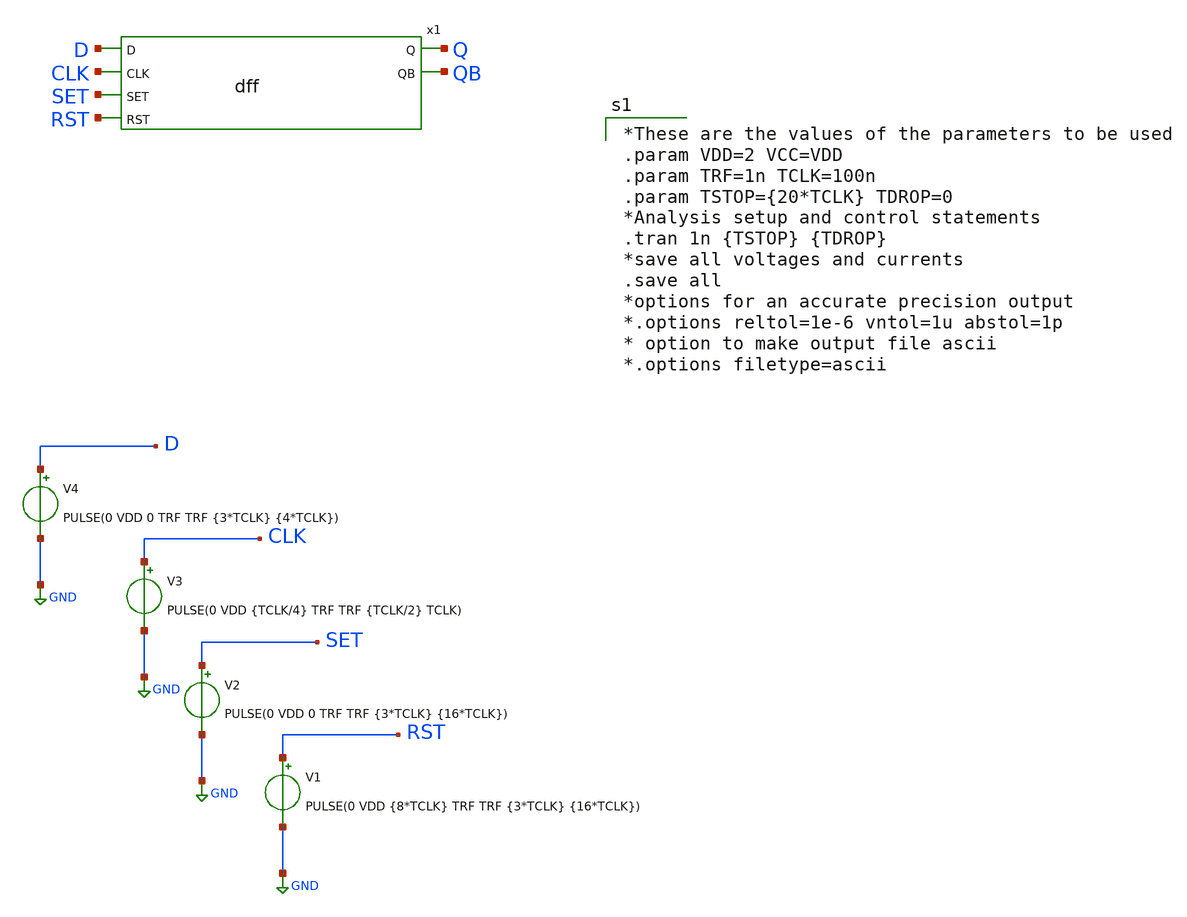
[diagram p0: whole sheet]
** sch_path: d_ff_test_bench.sch
**.subckt d_ff_test_bench
V1 RST GND PULSE(0 VDD {8*TCLK} TRF TRF {3*TCLK} {16*TCLK})
V2 SET GND PULSE(0 VDD 0 TRF TRF {3*TCLK} {16*TCLK})
V3 CLK GND PULSE(0 VDD {TCLK/4} TRF TRF {TCLK/2} TCLK)
V4 D GND PULSE(0 VDD 0 TRF TRF {3*TCLK} {4*TCLK})
x1 D CLK Q SET QB RST dff
**** begin user architecture code

*These are the values of the parameters to be used
.param VDD=2 VCC=VDD
.param TRF=1n TCLK=100n
.param TSTOP={20*TCLK} TDROP=0
*Analysis setup and control statements
.tran 1n {TSTOP} {TDROP}
*save all voltages and currents
.save all
*options for an accurate precision output
*.options reltol=1e-6 vntol=1u abstol=1p
* option to make output file ascii
*.options filetype=ascii


**** end user architecture code
**.ends

* expanding   symbol:  dff.sym # of pins=6
** sym_path: dff.sym
** sch_path: dff.sch
.subckt dff D CLK Q SET QB RST
*.ipin D
*.ipin CLK
*.ipin SET
*.ipin RST
*.opin Q
*.opin QB
**** begin user architecture code

a1 D CLK SET RST Qi QBi flop1
.model flop1 d_dff(clk_delay = 1e-9 set_delay = 1e-9  reset_delay = 1e-9 ic = 2 rise_delay = 1e-9
+  fall_delay = 1e-9)

v1 Qi Q 0
V2 QBi QB 0


**** end user architecture code
.ends

.GLOBAL GND
.end
